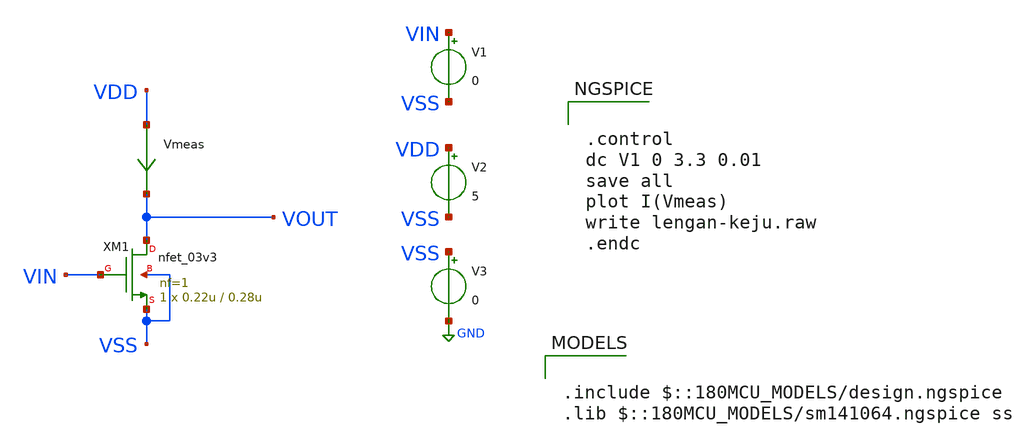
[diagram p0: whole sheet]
** sch_path: week02_current_diffpair/tugas5_cascode_current_mirror/lengan-keju.sch
**.subckt lengan-keju
XM1 VOUT VIN VSS VSS nfet_03v3 L=0.28u W=0.22u nf=1 ad='int((nf+1)/2) * W/nf * 0.18u' as='int((nf+2)/2) * W/nf * 0.18u'
+ pd='2*int((nf+1)/2) * (W/nf + 0.18u)' ps='2*int((nf+2)/2) * (W/nf + 0.18u)' nrd='0.18u / W' nrs='0.18u / W'
+ sa=0 sb=0 sd=0 m=1
V1 VIN VSS 0
V2 VDD VSS 5
V3 VSS GND 0
Vmeas VDD VOUT 0
.save i(vmeas)
**** begin user architecture code

.include $::180MCU_MODELS/design.ngspice
.lib $::180MCU_MODELS/sm141064.ngspice ss



.control
dc V1 0 3.3 0.01
save all
plot I(Vmeas)
write lengan-keju.raw
.endc


**** end user architecture code
**.ends
.GLOBAL GND
.end
